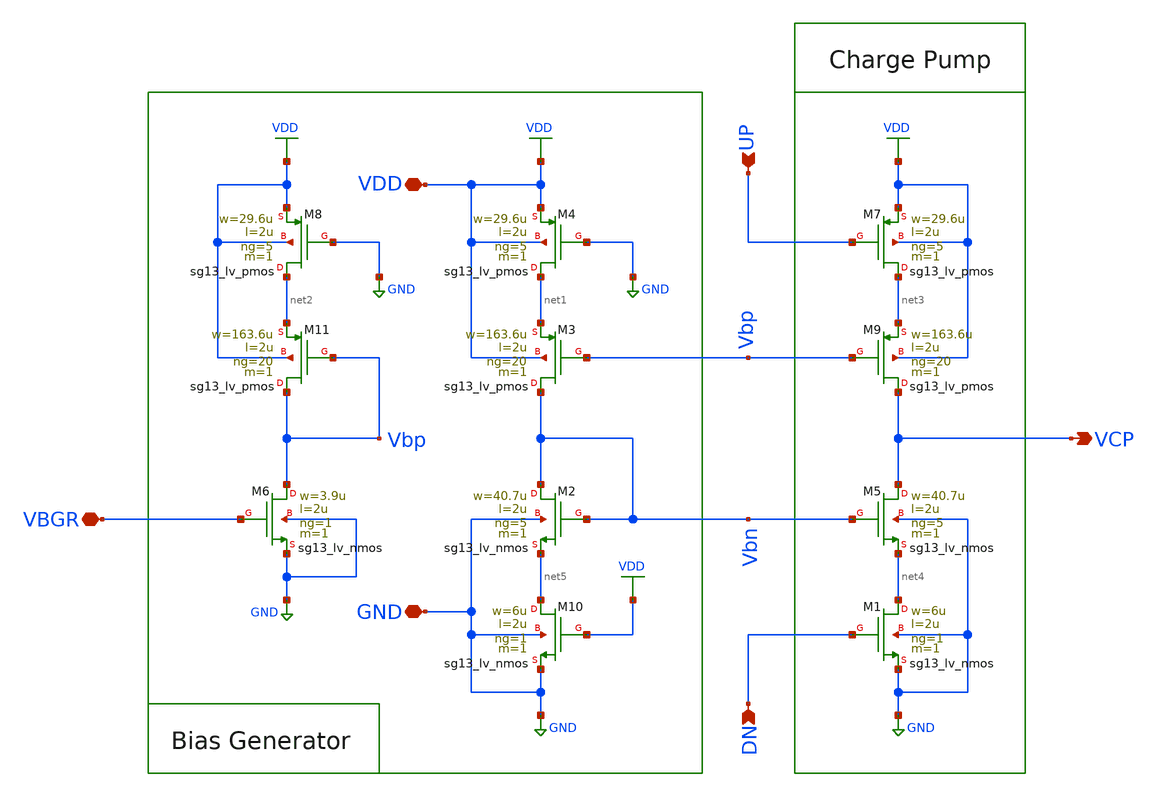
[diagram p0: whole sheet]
** sch_path: schematic/charge-pump/CHARGE_PUMP.sch
**.subckt CHARGE_PUMP VCP UP DN GND VBGR VDD
*.opin VCP
*.ipin UP
*.ipin DN
*.iopin GND
*.iopin VBGR
*.iopin VDD
XM2 Vbn Vbn net5 GND sg13_lv_nmos w=40.7u l=2u ng=5 m=1 mm_ok=1
XM8 net2 GND VDD VDD sg13_lv_pmos w=29.6u l=2u ng=5 m=1 mm_ok=1
XM11 Vbp Vbp net2 VDD sg13_lv_pmos w=163.6u l=2u ng=20 m=1 mm_ok=1
XM3 Vbn Vbp net1 VDD sg13_lv_pmos w=163.6u l=2u ng=20 m=1 mm_ok=1
XM4 net1 GND VDD VDD sg13_lv_pmos w=29.6u l=2u ng=5 m=1 mm_ok=1
XM7 net3 UP VDD VDD sg13_lv_pmos w=29.6u l=2u ng=5 m=1 mm_ok=1
XM9 VCP Vbp net3 VDD sg13_lv_pmos w=163.6u l=2u ng=20 m=1 mm_ok=1
XM10 net5 VDD GND GND sg13_lv_nmos w=6u l=2u ng=1 m=1 mm_ok=1
XM1 net4 DN GND GND sg13_lv_nmos w=6u l=2u ng=1 m=1 mm_ok=1
XM5 VCP Vbn net4 GND sg13_lv_nmos w=40.7u l=2u ng=5 m=1 mm_ok=1
XM6 Vbp VBGR GND GND sg13_lv_nmos w=3.9u l=2u ng=1 m=1 mm_ok=1
**.ends
.GLOBAL GND
.GLOBAL VDD
.end
